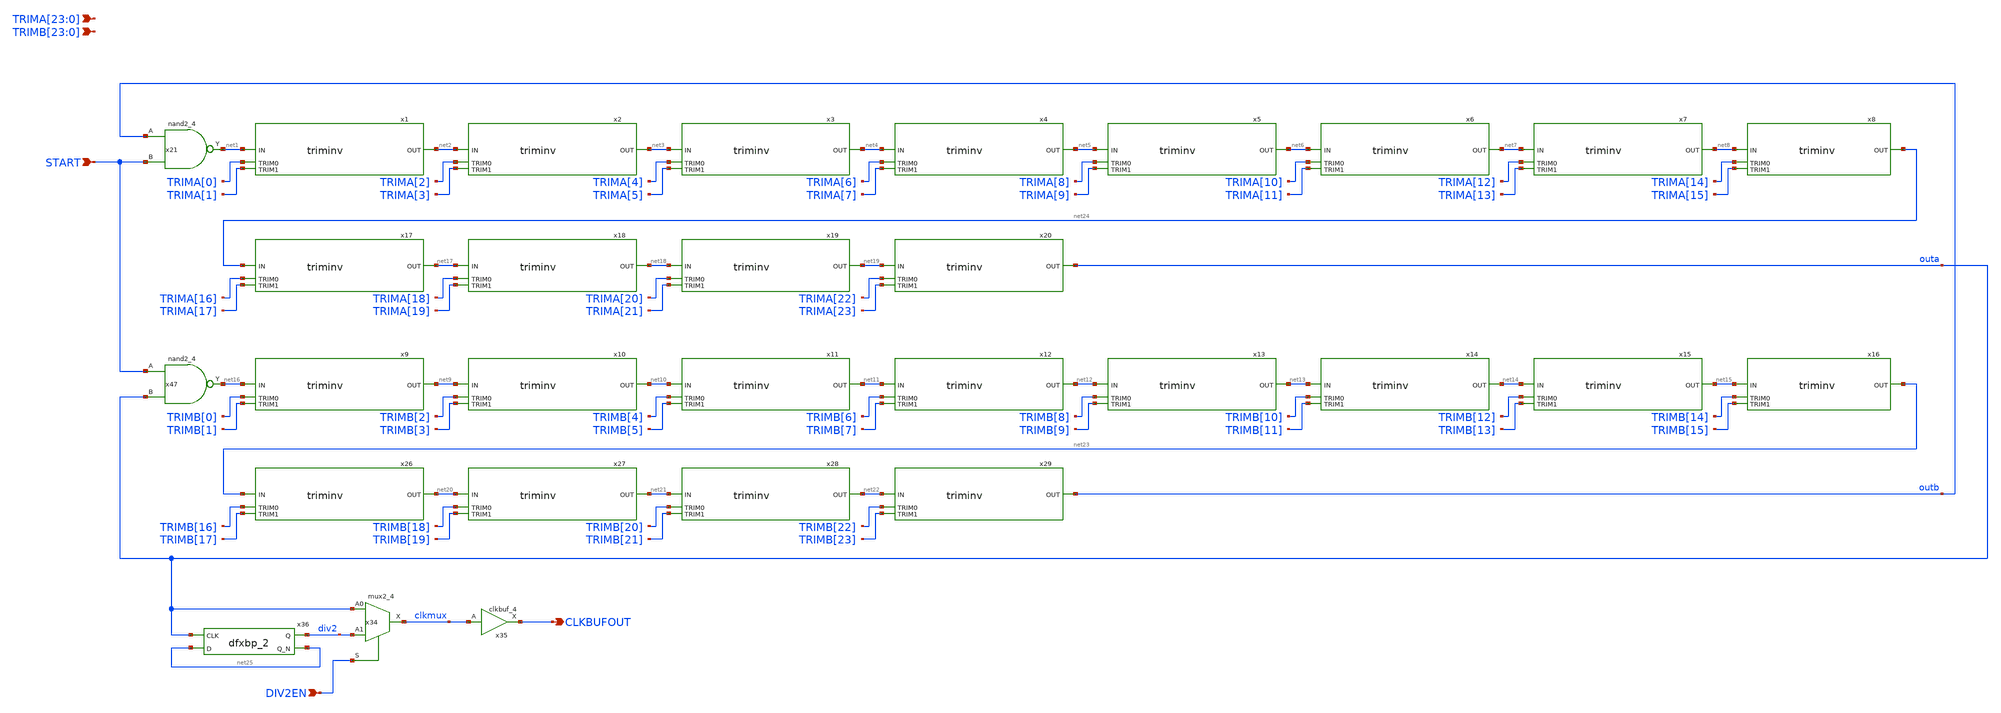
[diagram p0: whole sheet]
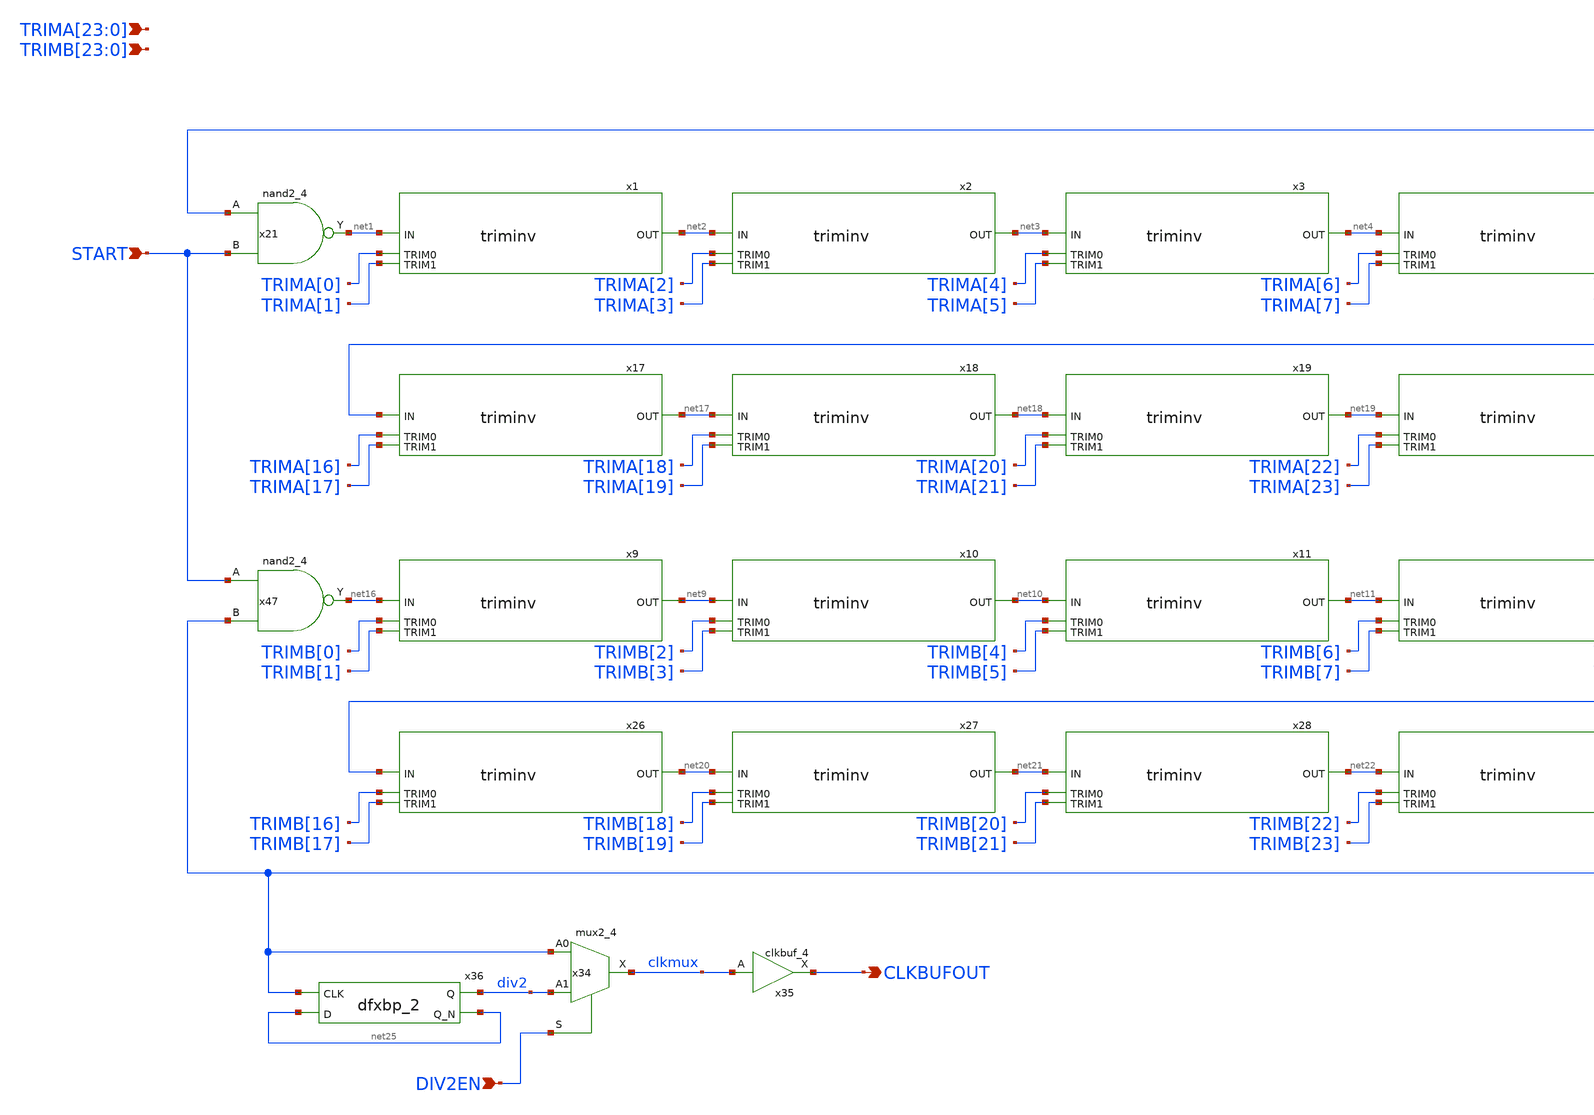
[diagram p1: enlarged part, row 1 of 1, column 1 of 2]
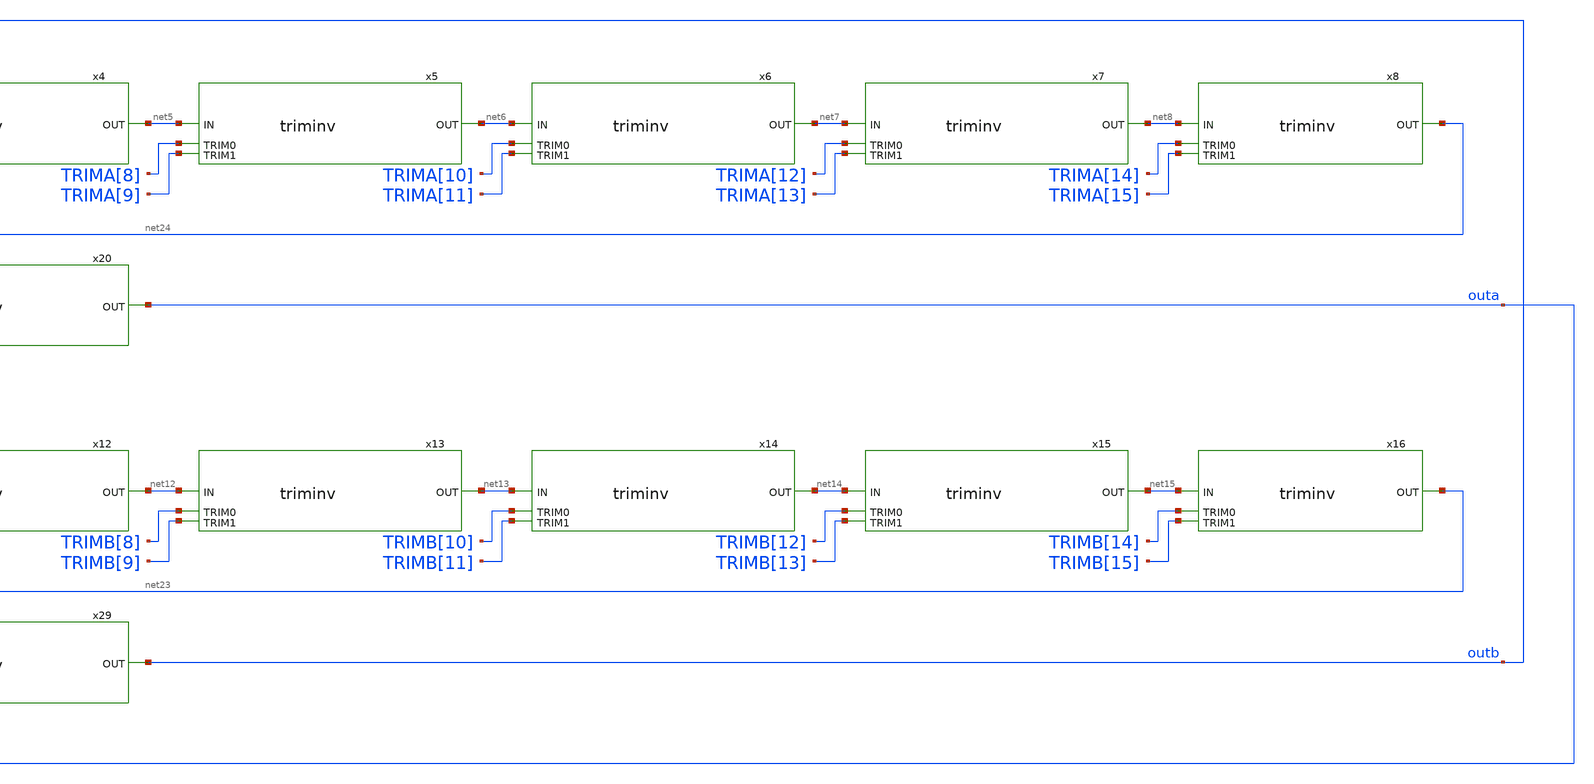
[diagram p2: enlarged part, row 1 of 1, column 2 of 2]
** sch_path: ip/randsack/sch/collapsering.sch
**.subckt collapsering CLKBUFOUT START DIV2EN
*+ TRIMA[23],TRIMA[22],TRIMA[21],TRIMA[20],TRIMA[19],TRIMA[18],TRIMA[17],TRIMA[16],TRIMA[15],TRIMA[14],TRIMA[13],TRIMA[12],TRIMA[11],TRIMA[10],TRIMA[9],TRIMA[8],TRIMA[7],TRIMA[6],TRIMA[5],TRIMA[4],TRIMA[3],TRIMA[2],TRIMA[1],TRIMA[0]
*+ TRIMB[23],TRIMB[22],TRIMB[21],TRIMB[20],TRIMB[19],TRIMB[18],TRIMB[17],TRIMB[16],TRIMB[15],TRIMB[14],TRIMB[13],TRIMB[12],TRIMB[11],TRIMB[10],TRIMB[9],TRIMB[8],TRIMB[7],TRIMB[6],TRIMB[5],TRIMB[4],TRIMB[3],TRIMB[2],TRIMB[1],TRIMB[0]
*.opin CLKBUFOUT
*.ipin START
*.ipin DIV2EN
*.ipin
*+ TRIMA[23],TRIMA[22],TRIMA[21],TRIMA[20],TRIMA[19],TRIMA[18],TRIMA[17],TRIMA[16],TRIMA[15],TRIMA[14],TRIMA[13],TRIMA[12],TRIMA[11],TRIMA[10],TRIMA[9],TRIMA[8],TRIMA[7],TRIMA[6],TRIMA[5],TRIMA[4],TRIMA[3],TRIMA[2],TRIMA[1],TRIMA[0]
*.ipin
*+ TRIMB[23],TRIMB[22],TRIMB[21],TRIMB[20],TRIMB[19],TRIMB[18],TRIMB[17],TRIMB[16],TRIMB[15],TRIMB[14],TRIMB[13],TRIMB[12],TRIMB[11],TRIMB[10],TRIMB[9],TRIMB[8],TRIMB[7],TRIMB[6],TRIMB[5],TRIMB[4],TRIMB[3],TRIMB[2],TRIMB[1],TRIMB[0]
x21 outb START VGND VNB VPB VPWR net1 sky130_fd_sc_hd__nand2_4
x47 START outa VGND VNB VPB VPWR net16 sky130_fd_sc_hd__nand2_4
x1 net2 net1 TRIMA[0] TRIMA[1] triminv
x2 net3 net2 TRIMA[2] TRIMA[3] triminv
x3 net4 net3 TRIMA[4] TRIMA[5] triminv
x4 net5 net4 TRIMA[6] TRIMA[7] triminv
x5 net6 net5 TRIMA[8] TRIMA[9] triminv
x6 net7 net6 TRIMA[10] TRIMA[11] triminv
x7 net8 net7 TRIMA[12] TRIMA[13] triminv
x8 net24 net8 TRIMA[14] TRIMA[15] triminv
x9 net9 net16 TRIMB[0] TRIMB[1] triminv
x10 net10 net9 TRIMB[2] TRIMB[3] triminv
x11 net11 net10 TRIMB[4] TRIMB[5] triminv
x12 net12 net11 TRIMB[6] TRIMB[7] triminv
x13 net13 net12 TRIMB[8] TRIMB[9] triminv
x14 net14 net13 TRIMB[10] TRIMB[11] triminv
x15 net15 net14 TRIMB[12] TRIMB[13] triminv
x16 net23 net15 TRIMB[14] TRIMB[15] triminv
x17 net17 net24 TRIMA[16] TRIMA[17] triminv
x18 net18 net17 TRIMA[18] TRIMA[19] triminv
x19 net19 net18 TRIMA[20] TRIMA[21] triminv
x20 outa net19 TRIMA[22] TRIMA[23] triminv
x26 net20 net23 TRIMB[16] TRIMB[17] triminv
x27 net21 net20 TRIMB[18] TRIMB[19] triminv
x28 net22 net21 TRIMB[20] TRIMB[21] triminv
x29 outb net22 TRIMB[22] TRIMB[23] triminv
x34 outa div2 DIV2EN VGND VNB VPB VPWR clkmux sky130_fd_sc_hd__mux2_4
x36 outa net25 VGND VNB VPB VPWR div2 net25 sky130_fd_sc_hd__dfxbp_2
x35 clkmux VGND VNB VPB VPWR CLKBUFOUT sky130_fd_sc_hd__clkbuf_4
**.ends

* expanding   symbol:  /home/harrison/workspace/randsack/verilog/rtl/randsack/sch/triminv.sym # of
*+ pins=4
** sym_path: ip/randsack/sch/triminv.sym
** sch_path: ip/randsack/sch/triminv.sch
.subckt triminv OUT IN TRIM0 TRIM1
*.ipin IN
*.ipin OUT
*.ipin TRIM0
*.ipin TRIM1
x1 IN VGND VNB VPB VPWR ts sky130_fd_sc_hd__clkbuf_2
x2 ts TRIM1 VGND VNB VPB VPWR d1 sky130_fd_sc_hd__einvn_4
x3 d1 VGND VNB VPB VPWR d2 sky130_fd_sc_hd__clkinv_1
x4 d2 TRIM0 VGND VNB VPB VPWR OUT sky130_fd_sc_hd__einvp_2
x5 ts VGND VNB VPB VPWR d0 sky130_fd_sc_hd__clkbuf_1
x6 d0 TRIM1 VGND VNB VPB VPWR d1 sky130_fd_sc_hd__einvp_2
x7 ts TRIM0 VGND VNB VPB VPWR OUT sky130_fd_sc_hd__einvn_8
.ends

.end
